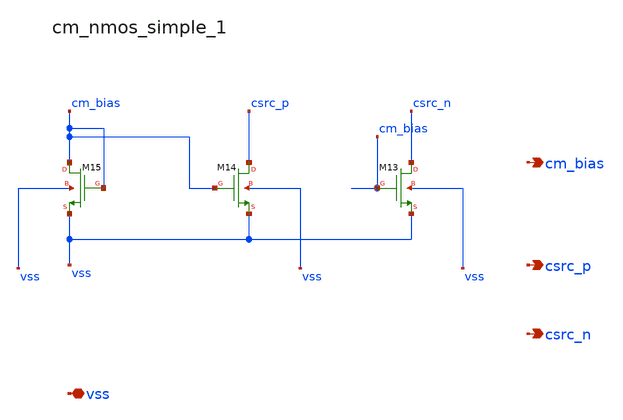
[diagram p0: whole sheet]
** sch_path: analog-db/raw/amp_027_fan_rrl_ota/hier/blocks/cm_nmos_simple_1.sch
**.subckt cm_nmos_simple_1 vss cm_bias csrc_p csrc_n
*.iopin vss
*.opin cm_bias
*.opin csrc_p
*.opin csrc_n
XM13 csrc_n cm_bias vss vss sg13_lv_nmos w=x_dut_xm13_w l=x_dut_xm13_l ng=1 m=x_dut_xm13_m
XM14 csrc_p cm_bias vss vss sg13_lv_nmos w=x_dut_xm14_w l=x_dut_xm14_l ng=1 m=x_dut_xm14_m
XM15 cm_bias cm_bias vss vss sg13_lv_nmos w=x_dut_xm15_w l=x_dut_xm15_l ng=1 m=x_dut_xm15_m
**.ends
.end
